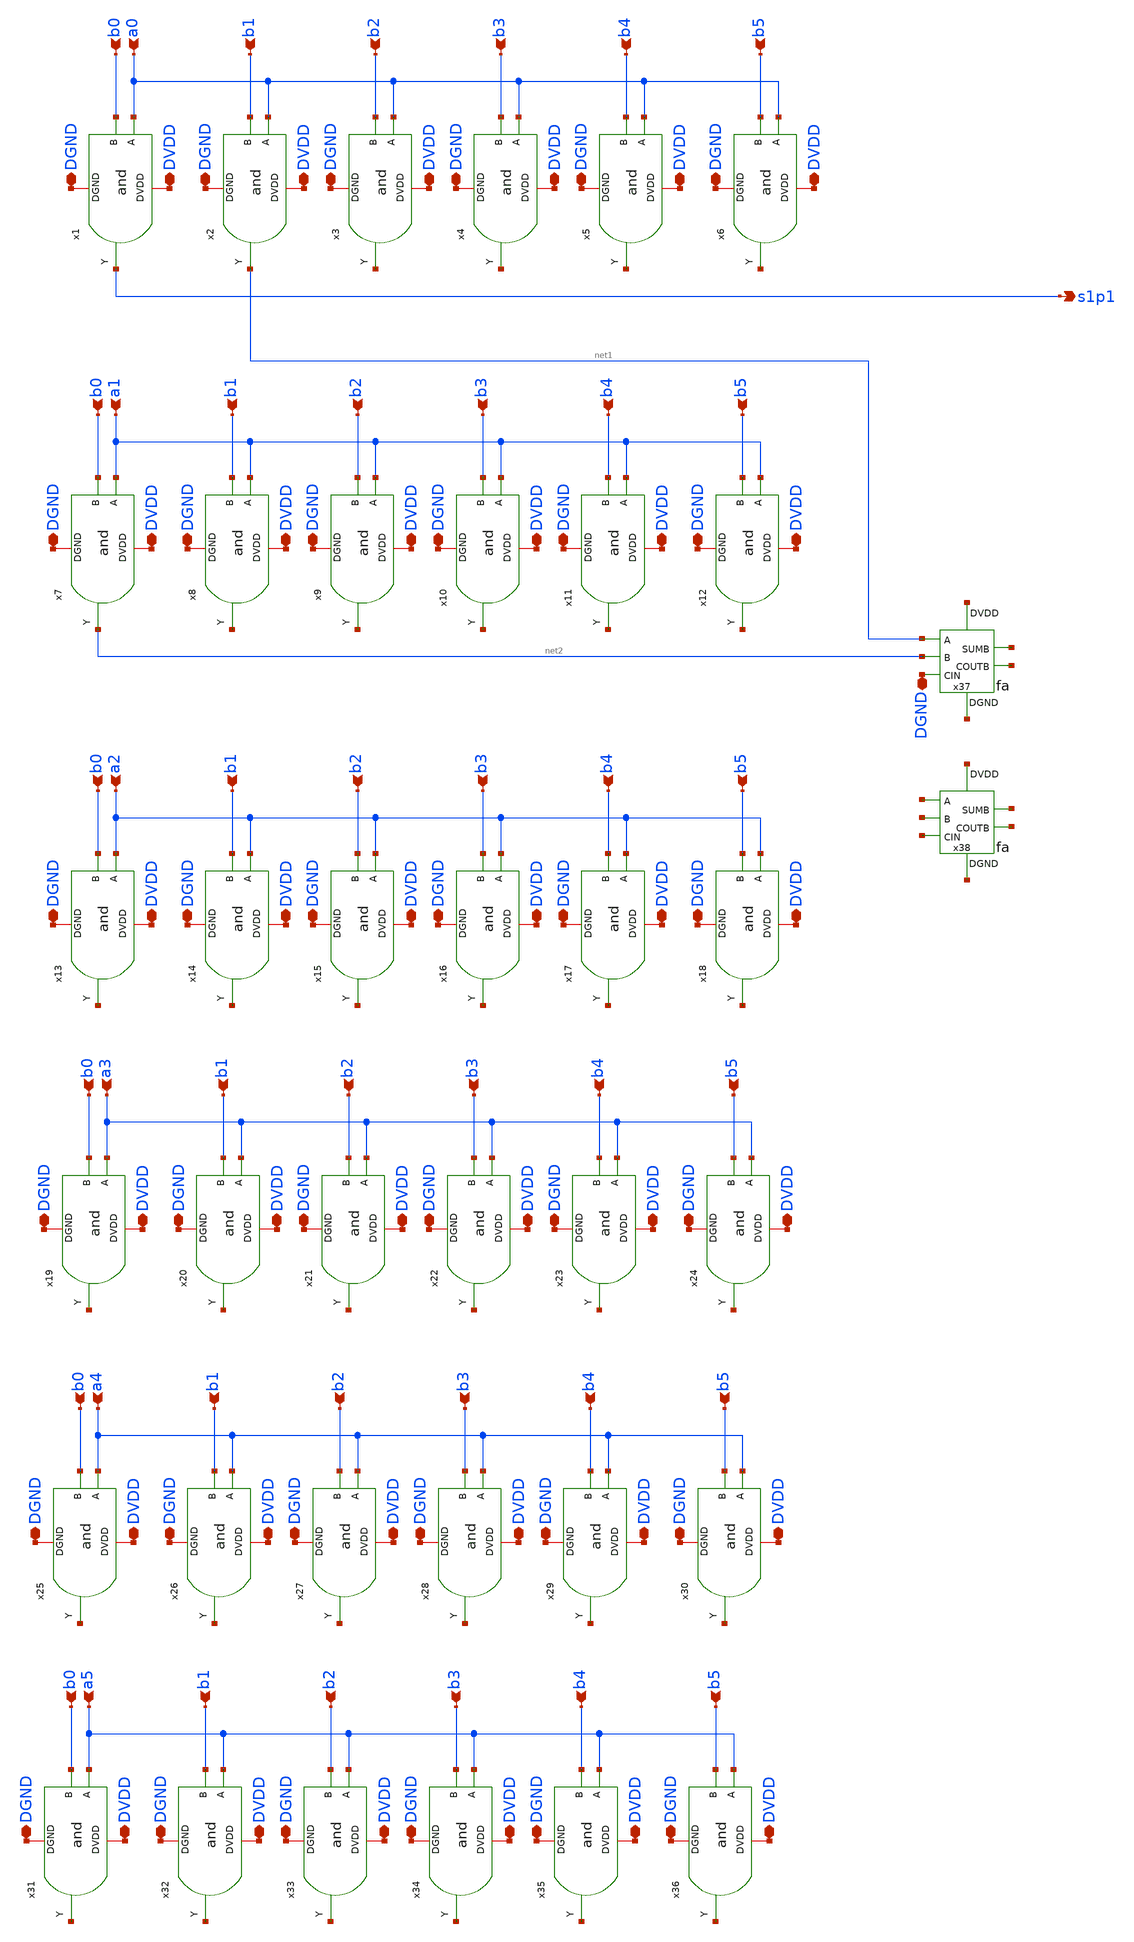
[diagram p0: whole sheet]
** sch_path: project/sch_sym_files/stage1.sch
**.subckt stage1 a0 a1 b0 b2 b3 b4 b5 b1 DVDD DGND DGND DGND DGND DGND DGND DVDD DVDD DVDD DVDD DVDD
*+ b0 b2 b3 b4 b5 b1 DVDD DGND DGND DGND DGND DGND DGND DVDD DVDD DVDD DVDD DVDD a2 b0 b2 b3 b4 b5 b1
*+ DVDD DGND DGND DGND DGND DGND DGND DVDD DVDD DVDD DVDD DVDD a3 b0 b2 b3 b4 b5 b1 DVDD DGND DGND DGND
*+ DGND DGND DGND DVDD DVDD DVDD DVDD DVDD a4 b0 b2 b3 b4 b5 b1 DVDD DGND DGND DGND DGND DGND DGND DVDD
*+ DVDD DVDD DVDD DVDD a5 b0 b2 b3 b4 b5 b1 DVDD DGND DGND DGND DGND DGND DGND DVDD DVDD DVDD DVDD DVDD
*+ s1p1 DGND
*.ipin a0
*.ipin a1
*.ipin b0
*.ipin b2
*.ipin b3
*.ipin b4
*.ipin b5
*.ipin b1
*.iopin DVDD
*.iopin DGND
*.iopin DGND
*.iopin DGND
*.iopin DGND
*.iopin DGND
*.iopin DGND
*.iopin DVDD
*.iopin DVDD
*.iopin DVDD
*.iopin DVDD
*.iopin DVDD
*.ipin b0
*.ipin b2
*.ipin b3
*.ipin b4
*.ipin b5
*.ipin b1
*.iopin DVDD
*.iopin DGND
*.iopin DGND
*.iopin DGND
*.iopin DGND
*.iopin DGND
*.iopin DGND
*.iopin DVDD
*.iopin DVDD
*.iopin DVDD
*.iopin DVDD
*.iopin DVDD
*.ipin a2
*.ipin b0
*.ipin b2
*.ipin b3
*.ipin b4
*.ipin b5
*.ipin b1
*.iopin DVDD
*.iopin DGND
*.iopin DGND
*.iopin DGND
*.iopin DGND
*.iopin DGND
*.iopin DGND
*.iopin DVDD
*.iopin DVDD
*.iopin DVDD
*.iopin DVDD
*.iopin DVDD
*.ipin a3
*.ipin b0
*.ipin b2
*.ipin b3
*.ipin b4
*.ipin b5
*.ipin b1
*.iopin DVDD
*.iopin DGND
*.iopin DGND
*.iopin DGND
*.iopin DGND
*.iopin DGND
*.iopin DGND
*.iopin DVDD
*.iopin DVDD
*.iopin DVDD
*.iopin DVDD
*.iopin DVDD
*.ipin a4
*.ipin b0
*.ipin b2
*.ipin b3
*.ipin b4
*.ipin b5
*.ipin b1
*.iopin DVDD
*.iopin DGND
*.iopin DGND
*.iopin DGND
*.iopin DGND
*.iopin DGND
*.iopin DGND
*.iopin DVDD
*.iopin DVDD
*.iopin DVDD
*.iopin DVDD
*.iopin DVDD
*.ipin a5
*.ipin b0
*.ipin b2
*.ipin b3
*.ipin b4
*.ipin b5
*.ipin b1
*.iopin DVDD
*.iopin DGND
*.iopin DGND
*.iopin DGND
*.iopin DGND
*.iopin DGND
*.iopin DGND
*.iopin DVDD
*.iopin DVDD
*.iopin DVDD
*.iopin DVDD
*.iopin DVDD
*.opin s1p1
*.iopin DGND
x1 DVDD a0 s1p1 b0 DGND and
x2 DVDD a0 net1 b1 DGND and
x3 DVDD a0 net3 b2 DGND and
x4 DVDD a0 net4 b3 DGND and
x5 DVDD a0 net5 b4 DGND and
x6 DVDD a0 net6 b5 DGND and
x7 DVDD a1 net2 b0 DGND and
x8 DVDD a1 net7 b1 DGND and
x9 DVDD a1 net8 b2 DGND and
x10 DVDD a1 net9 b3 DGND and
x11 DVDD a1 net10 b4 DGND and
x12 DVDD a1 net11 b5 DGND and
x13 DVDD a2 net12 b0 DGND and
x14 DVDD a2 net13 b1 DGND and
x15 DVDD a2 net14 b2 DGND and
x16 DVDD a2 net15 b3 DGND and
x17 DVDD a2 net16 b4 DGND and
x18 DVDD a2 net17 b5 DGND and
x19 DVDD a3 net18 b0 DGND and
x20 DVDD a3 net19 b1 DGND and
x21 DVDD a3 net20 b2 DGND and
x22 DVDD a3 net21 b3 DGND and
x23 DVDD a3 net22 b4 DGND and
x24 DVDD a3 net23 b5 DGND and
x25 DVDD a4 net24 b0 DGND and
x26 DVDD a4 net25 b1 DGND and
x27 DVDD a4 net26 b2 DGND and
x28 DVDD a4 net27 b3 DGND and
x29 DVDD a4 net28 b4 DGND and
x30 DVDD a4 net29 b5 DGND and
x31 DVDD a5 net30 b0 DGND and
x32 DVDD a5 net31 b1 DGND and
x33 DVDD a5 net32 b2 DGND and
x34 DVDD a5 net33 b3 DGND and
x35 DVDD a5 net34 b4 DGND and
x36 DVDD a5 net35 b5 DGND and
x37 net36 net37 net1 net2 DGND net38 net39 fa
x38 net40 net41 net42 net43 net44 net45 net46 fa
**.ends

* expanding   symbol:  and.sym # of pins=5
** sym_path: project/sch_sym_files/and.sym
** sch_path: project/sch_sym_files/and.sch
.subckt and DVDD A Y B DGND
*.ipin A
*.ipin B
*.opin Y
*.iopin DVDD
*.iopin DGND
x1 DVDD A B net1 DGND nand2
x2 net1 Y net2 net3 inv
.ends


* expanding   symbol:  fa.sym # of pins=7
** sym_path: project/sch_sym_files/fa.sym
** sch_path: project/sch_sym_files/fa.sch
.subckt fa DVDD DGND A B CIN COUTB SUMB
*.opin COUTB
*.ipin CIN
*.iopin DVDD
*.iopin DGND
*.opin SUMB
*.ipin B
*.ipin A
XM3 SUMB CIN net4 DGND sky130_fd_pr__nfet_01v8 L=0.15 W=0.42 nf=1 ad='int((nf+1)/2) * W/nf * 0.29' as='int((nf+2)/2) * W/nf * 0.29'
+ pd='2*int((nf+1)/2) * (W/nf + 0.29)' ps='2*int((nf+2)/2) * (W/nf + 0.29)' nrd='0.29 / W' nrs='0.29 / W'
+ sa=0 sb=0 sd=0 mult=1 m=1
XM1 net2 A DVDD DVDD sky130_fd_pr__pfet_01v8 L=0.15 W=0.42 nf=1 ad='int((nf+1)/2) * W/nf * 0.29' as='int((nf+2)/2) * W/nf * 0.29'
+ pd='2*int((nf+1)/2) * (W/nf + 0.29)' ps='2*int((nf+2)/2) * (W/nf + 0.29)' nrd='0.29 / W' nrs='0.29 / W'
+ sa=0 sb=0 sd=0 mult=1 m=1
XM2 net1 B net2 DVDD sky130_fd_pr__pfet_01v8 L=0.15 W=0.42 nf=1 ad='int((nf+1)/2) * W/nf * 0.29' as='int((nf+2)/2) * W/nf * 0.29'
+ pd='2*int((nf+1)/2) * (W/nf + 0.29)' ps='2*int((nf+2)/2) * (W/nf + 0.29)' nrd='0.29 / W' nrs='0.29 / W'
+ sa=0 sb=0 sd=0 mult=1 m=1
XM4 SUMB CIN net1 DVDD sky130_fd_pr__pfet_01v8 L=0.15 W=0.42 nf=1 ad='int((nf+1)/2) * W/nf * 0.29' as='int((nf+2)/2) * W/nf * 0.29'
+ pd='2*int((nf+1)/2) * (W/nf + 0.29)' ps='2*int((nf+2)/2) * (W/nf + 0.29)' nrd='0.29 / W' nrs='0.29 / W'
+ sa=0 sb=0 sd=0 mult=1 m=1
XM5 net4 B net3 DGND sky130_fd_pr__nfet_01v8 L=0.15 W=0.42 nf=1 ad='int((nf+1)/2) * W/nf * 0.29' as='int((nf+2)/2) * W/nf * 0.29'
+ pd='2*int((nf+1)/2) * (W/nf + 0.29)' ps='2*int((nf+2)/2) * (W/nf + 0.29)' nrd='0.29 / W' nrs='0.29 / W'
+ sa=0 sb=0 sd=0 mult=1 m=1
XM6 net3 A DGND DGND sky130_fd_pr__nfet_01v8 L=0.15 W=0.42 nf=1 ad='int((nf+1)/2) * W/nf * 0.29' as='int((nf+2)/2) * W/nf * 0.29'
+ pd='2*int((nf+1)/2) * (W/nf + 0.29)' ps='2*int((nf+2)/2) * (W/nf + 0.29)' nrd='0.29 / W' nrs='0.29 / W'
+ sa=0 sb=0 sd=0 mult=1 m=1
XM7 net5 A DVDD DVDD sky130_fd_pr__pfet_01v8 L=0.15 W=0.42 nf=1 ad='int((nf+1)/2) * W/nf * 0.29' as='int((nf+2)/2) * W/nf * 0.29'
+ pd='2*int((nf+1)/2) * (W/nf + 0.29)' ps='2*int((nf+2)/2) * (W/nf + 0.29)' nrd='0.29 / W' nrs='0.29 / W'
+ sa=0 sb=0 sd=0 mult=1 m=1
XM8 net5 B DVDD DVDD sky130_fd_pr__pfet_01v8 L=0.15 W=0.42 nf=1 ad='int((nf+1)/2) * W/nf * 0.29' as='int((nf+2)/2) * W/nf * 0.29'
+ pd='2*int((nf+1)/2) * (W/nf + 0.29)' ps='2*int((nf+2)/2) * (W/nf + 0.29)' nrd='0.29 / W' nrs='0.29 / W'
+ sa=0 sb=0 sd=0 mult=1 m=1
XM9 net5 CIN DVDD DVDD sky130_fd_pr__pfet_01v8 L=0.15 W=0.42 nf=1 ad='int((nf+1)/2) * W/nf * 0.29' as='int((nf+2)/2) * W/nf * 0.29'
+ pd='2*int((nf+1)/2) * (W/nf + 0.29)' ps='2*int((nf+2)/2) * (W/nf + 0.29)' nrd='0.29 / W' nrs='0.29 / W'
+ sa=0 sb=0 sd=0 mult=1 m=1
XM10 SUMB COUTB net5 DVDD sky130_fd_pr__pfet_01v8 L=0.15 W=0.42 nf=1 ad='int((nf+1)/2) * W/nf * 0.29'
+ as='int((nf+2)/2) * W/nf * 0.29' pd='2*int((nf+1)/2) * (W/nf + 0.29)' ps='2*int((nf+2)/2) * (W/nf + 0.29)'
+ nrd='0.29 / W' nrs='0.29 / W' sa=0 sb=0 sd=0 mult=1 m=1
XM11 net6 A DGND DGND sky130_fd_pr__nfet_01v8 L=0.15 W=0.42 nf=1 ad='int((nf+1)/2) * W/nf * 0.29' as='int((nf+2)/2) * W/nf * 0.29'
+ pd='2*int((nf+1)/2) * (W/nf + 0.29)' ps='2*int((nf+2)/2) * (W/nf + 0.29)' nrd='0.29 / W' nrs='0.29 / W'
+ sa=0 sb=0 sd=0 mult=1 m=1
XM12 net6 B DGND DGND sky130_fd_pr__nfet_01v8 L=0.15 W=0.42 nf=1 ad='int((nf+1)/2) * W/nf * 0.29' as='int((nf+2)/2) * W/nf * 0.29'
+ pd='2*int((nf+1)/2) * (W/nf + 0.29)' ps='2*int((nf+2)/2) * (W/nf + 0.29)' nrd='0.29 / W' nrs='0.29 / W'
+ sa=0 sb=0 sd=0 mult=1 m=1
XM13 net6 CIN DGND DGND sky130_fd_pr__nfet_01v8 L=0.15 W=0.42 nf=1 ad='int((nf+1)/2) * W/nf * 0.29' as='int((nf+2)/2) * W/nf * 0.29'
+ pd='2*int((nf+1)/2) * (W/nf + 0.29)' ps='2*int((nf+2)/2) * (W/nf + 0.29)' nrd='0.29 / W' nrs='0.29 / W'
+ sa=0 sb=0 sd=0 mult=1 m=1
XM14 SUMB COUTB net6 DGND sky130_fd_pr__nfet_01v8 L=0.15 W=0.42 nf=1 ad='int((nf+1)/2) * W/nf * 0.29'
+ as='int((nf+2)/2) * W/nf * 0.29' pd='2*int((nf+1)/2) * (W/nf + 0.29)' ps='2*int((nf+2)/2) * (W/nf + 0.29)'
+ nrd='0.29 / W' nrs='0.29 / W' sa=0 sb=0 sd=0 mult=1 m=1
XM15 COUTB CIN net10 DGND sky130_fd_pr__nfet_01v8 L=0.15 W=0.42 nf=1 ad='int((nf+1)/2) * W/nf * 0.29'
+ as='int((nf+2)/2) * W/nf * 0.29' pd='2*int((nf+1)/2) * (W/nf + 0.29)' ps='2*int((nf+2)/2) * (W/nf + 0.29)'
+ nrd='0.29 / W' nrs='0.29 / W' sa=0 sb=0 sd=0 mult=1 m=1
XM16 net7 A DVDD DVDD sky130_fd_pr__pfet_01v8 L=0.15 W=0.42 nf=1 ad='int((nf+1)/2) * W/nf * 0.29' as='int((nf+2)/2) * W/nf * 0.29'
+ pd='2*int((nf+1)/2) * (W/nf + 0.29)' ps='2*int((nf+2)/2) * (W/nf + 0.29)' nrd='0.29 / W' nrs='0.29 / W'
+ sa=0 sb=0 sd=0 mult=1 m=1
XM17 COUTB B net7 DVDD sky130_fd_pr__pfet_01v8 L=0.15 W=0.42 nf=1 ad='int((nf+1)/2) * W/nf * 0.29' as='int((nf+2)/2) * W/nf * 0.29'
+ pd='2*int((nf+1)/2) * (W/nf + 0.29)' ps='2*int((nf+2)/2) * (W/nf + 0.29)' nrd='0.29 / W' nrs='0.29 / W'
+ sa=0 sb=0 sd=0 mult=1 m=1
XM18 COUTB CIN net9 DVDD sky130_fd_pr__pfet_01v8 L=0.15 W=0.42 nf=1 ad='int((nf+1)/2) * W/nf * 0.29'
+ as='int((nf+2)/2) * W/nf * 0.29' pd='2*int((nf+1)/2) * (W/nf + 0.29)' ps='2*int((nf+2)/2) * (W/nf + 0.29)'
+ nrd='0.29 / W' nrs='0.29 / W' sa=0 sb=0 sd=0 mult=1 m=1
XM19 COUTB B net8 DGND sky130_fd_pr__nfet_01v8 L=0.15 W=0.42 nf=1 ad='int((nf+1)/2) * W/nf * 0.29' as='int((nf+2)/2) * W/nf * 0.29'
+ pd='2*int((nf+1)/2) * (W/nf + 0.29)' ps='2*int((nf+2)/2) * (W/nf + 0.29)' nrd='0.29 / W' nrs='0.29 / W'
+ sa=0 sb=0 sd=0 mult=1 m=1
XM20 net8 A DGND DGND sky130_fd_pr__nfet_01v8 L=0.15 W=0.42 nf=1 ad='int((nf+1)/2) * W/nf * 0.29' as='int((nf+2)/2) * W/nf * 0.29'
+ pd='2*int((nf+1)/2) * (W/nf + 0.29)' ps='2*int((nf+2)/2) * (W/nf + 0.29)' nrd='0.29 / W' nrs='0.29 / W'
+ sa=0 sb=0 sd=0 mult=1 m=1
XM21 net9 A DVDD DVDD sky130_fd_pr__pfet_01v8 L=0.15 W=0.42 nf=1 ad='int((nf+1)/2) * W/nf * 0.29' as='int((nf+2)/2) * W/nf * 0.29'
+ pd='2*int((nf+1)/2) * (W/nf + 0.29)' ps='2*int((nf+2)/2) * (W/nf + 0.29)' nrd='0.29 / W' nrs='0.29 / W'
+ sa=0 sb=0 sd=0 mult=1 m=1
XM22 net9 B DVDD DVDD sky130_fd_pr__pfet_01v8 L=0.15 W=0.42 nf=1 ad='int((nf+1)/2) * W/nf * 0.29' as='int((nf+2)/2) * W/nf * 0.29'
+ pd='2*int((nf+1)/2) * (W/nf + 0.29)' ps='2*int((nf+2)/2) * (W/nf + 0.29)' nrd='0.29 / W' nrs='0.29 / W'
+ sa=0 sb=0 sd=0 mult=1 m=1
XM23 net10 A DGND DGND sky130_fd_pr__nfet_01v8 L=0.15 W=0.42 nf=1 ad='int((nf+1)/2) * W/nf * 0.29' as='int((nf+2)/2) * W/nf * 0.29'
+ pd='2*int((nf+1)/2) * (W/nf + 0.29)' ps='2*int((nf+2)/2) * (W/nf + 0.29)' nrd='0.29 / W' nrs='0.29 / W'
+ sa=0 sb=0 sd=0 mult=1 m=1
XM24 net10 B DGND DGND sky130_fd_pr__nfet_01v8 L=0.15 W=0.42 nf=1 ad='int((nf+1)/2) * W/nf * 0.29' as='int((nf+2)/2) * W/nf * 0.29'
+ pd='2*int((nf+1)/2) * (W/nf + 0.29)' ps='2*int((nf+2)/2) * (W/nf + 0.29)' nrd='0.29 / W' nrs='0.29 / W'
+ sa=0 sb=0 sd=0 mult=1 m=1
.ends


* expanding   symbol:  nand2.sym # of pins=5
** sym_path: project/sch_sym_files/nand2.sym
** sch_path: project/sch_sym_files/nand2.sch
.subckt nand2 DVDD A B Y DGND
*.opin Y
*.ipin A
*.iopin DVDD
*.iopin DGND
*.ipin B
XM2 Y A DVDD DVDD sky130_fd_pr__pfet_01v8 L=0.15 W=1.00 nf=1 ad='int((nf+1)/2) * W/nf * 0.29' as='int((nf+2)/2) * W/nf * 0.29'
+ pd='2*int((nf+1)/2) * (W/nf + 0.29)' ps='2*int((nf+2)/2) * (W/nf + 0.29)' nrd='0.29 / W' nrs='0.29 / W'
+ sa=0 sb=0 sd=0 mult=1 m=1
XM1 Y A net1 DGND sky130_fd_pr__nfet_01v8 L=0.15 W=0.65 nf=1 ad='int((nf+1)/2) * W/nf * 0.29' as='int((nf+2)/2) * W/nf * 0.29'
+ pd='2*int((nf+1)/2) * (W/nf + 0.29)' ps='2*int((nf+2)/2) * (W/nf + 0.29)' nrd='0.29 / W' nrs='0.29 / W'
+ sa=0 sb=0 sd=0 mult=1 m=1
XM3 net1 B DGND DGND sky130_fd_pr__nfet_01v8 L=0.15 W=0.65 nf=1 ad='int((nf+1)/2) * W/nf * 0.29' as='int((nf+2)/2) * W/nf * 0.29'
+ pd='2*int((nf+1)/2) * (W/nf + 0.29)' ps='2*int((nf+2)/2) * (W/nf + 0.29)' nrd='0.29 / W' nrs='0.29 / W'
+ sa=0 sb=0 sd=0 mult=1 m=1
XM7 Y B DVDD DVDD sky130_fd_pr__pfet_01v8 L=0.15 W=1.00 nf=1 ad='int((nf+1)/2) * W/nf * 0.29' as='int((nf+2)/2) * W/nf * 0.29'
+ pd='2*int((nf+1)/2) * (W/nf + 0.29)' ps='2*int((nf+2)/2) * (W/nf + 0.29)' nrd='0.29 / W' nrs='0.29 / W'
+ sa=0 sb=0 sd=0 mult=1 m=1
.ends


* expanding   symbol:  inv.sym # of pins=4
** sym_path: project/sch_sym_files/inv.sym
** sch_path: project/sch_sym_files/inv.sch
.subckt inv A Y DVDD DGND
*.opin Y
*.ipin A
*.iopin DVDD
*.iopin DGND
XM2 Y A DVDD DVDD sky130_fd_pr__pfet_01v8 L=0.15 W=1.00 nf=1 ad='int((nf+1)/2) * W/nf * 0.29' as='int((nf+2)/2) * W/nf * 0.29'
+ pd='2*int((nf+1)/2) * (W/nf + 0.29)' ps='2*int((nf+2)/2) * (W/nf + 0.29)' nrd='0.29 / W' nrs='0.29 / W'
+ sa=0 sb=0 sd=0 mult=1 m=1
XM1 Y A DGND DGND sky130_fd_pr__nfet_01v8 L=0.15 W=0.65 nf=1 ad='int((nf+1)/2) * W/nf * 0.29' as='int((nf+2)/2) * W/nf * 0.29'
+ pd='2*int((nf+1)/2) * (W/nf + 0.29)' ps='2*int((nf+2)/2) * (W/nf + 0.29)' nrd='0.29 / W' nrs='0.29 / W'
+ sa=0 sb=0 sd=0 mult=1 m=1
.ends

.end
